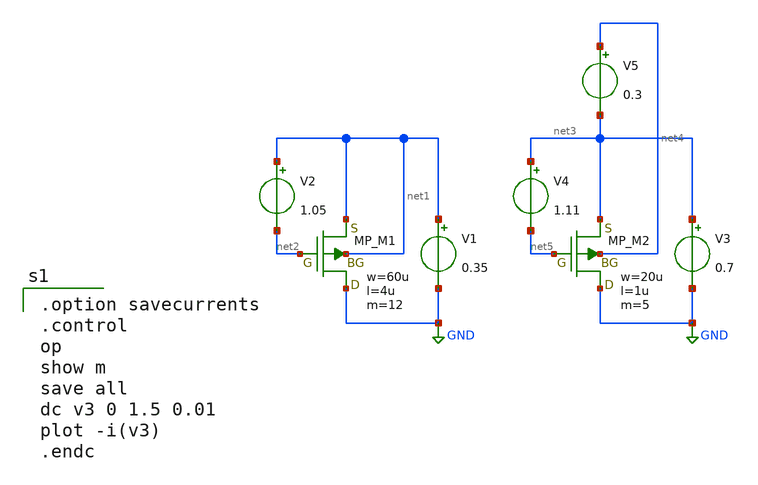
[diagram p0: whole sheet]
** sch_path: member_project/DCDC/ShuntaroOHNO/xschem/pmos_id_bias.sch
**.subckt pmos_id_bias
XM1 GND net2 net1 net1 PMOS w=60u l=4u as=0 ad=0 ps=0 pd=0 nrd=0 nrs=0 m=12
V1 net1 GND 0.35
V2 net1 net2 1.05
XM2 GND net5 net3 net4 PMOS w=20u l=1u as=0 ad=0 ps=0 pd=0 nrd=0 nrs=0 m=5
V3 net3 GND 0.7
V4 net3 net5 1.11
V5 net4 net3 0.3
**** begin user architecture code
 .include $::LIB/ip62_models

.option savecurrents
.control
op
show m
save all
dc v3 0 1.5 0.01
plot -i(v3)
.endc

**** end user architecture code
**.ends
.GLOBAL GND
.end
